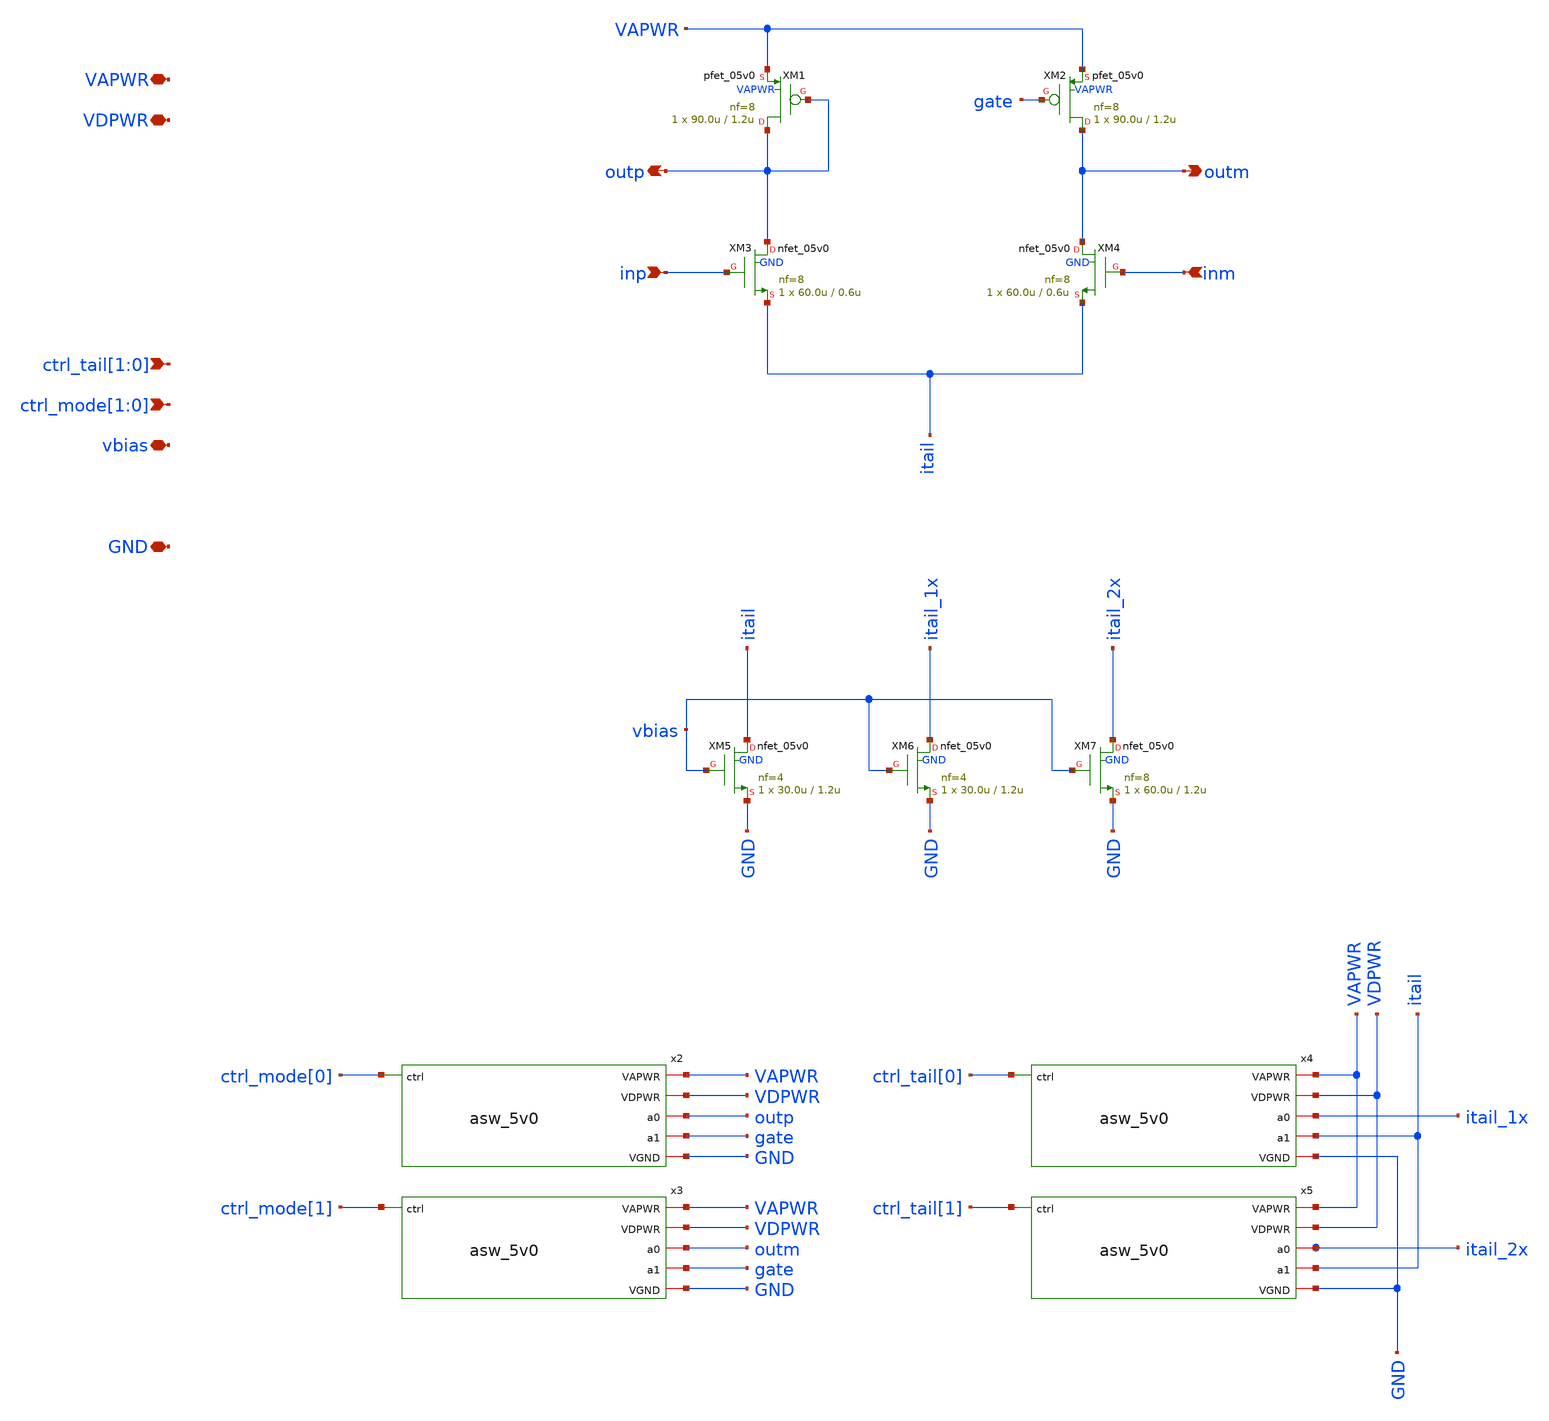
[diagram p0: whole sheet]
** sch_path: xschem/ota_n.sch
**.subckt ota_n vbias ctrl_tail[1],ctrl_tail[0] VAPWR VDPWR GND ctrl_mode[1],ctrl_mode[0] inp inm
*+ outp outm
*.iopin vbias
*.ipin ctrl_tail[1],ctrl_tail[0]
*.iopin VAPWR
*.iopin VDPWR
*.iopin GND
*.ipin ctrl_mode[1],ctrl_mode[0]
*.ipin inp
*.ipin inm
*.opin outp
*.opin outm
x2 GND VDPWR VAPWR ctrl_mode[0] outp gate asw_5v0
x3 GND VDPWR VAPWR ctrl_mode[1] outm gate asw_5v0
x4 GND VDPWR VAPWR ctrl_tail[0] itail_1x itail asw_5v0
x5 GND VDPWR VAPWR ctrl_tail[1] itail_2x itail asw_5v0
XM5 itail vbias GND GND nfet_05v0 L=1.2u W=30.0u nf=4 ad='int((nf+1)/2) * W/nf * 0.18u' as='int((nf+2)/2) * W/nf * 0.18u'
+ pd='2*int((nf+1)/2) * (W/nf + 0.18u)' ps='2*int((nf+2)/2) * (W/nf + 0.18u)' nrd='0.18u / W' nrs='0.18u / W'
+ sa=0 sb=0 sd=0 m=1 par=1
XM6 itail_1x vbias GND GND nfet_05v0 L=1.2u W=30.0u nf=4 ad='int((nf+1)/2) * W/nf * 0.18u' as='int((nf+2)/2) * W/nf * 0.18u'
+ pd='2*int((nf+1)/2) * (W/nf + 0.18u)' ps='2*int((nf+2)/2) * (W/nf + 0.18u)' nrd='0.18u / W' nrs='0.18u / W'
+ sa=0 sb=0 sd=0 m=1 par=1
XM7 itail_2x vbias GND GND nfet_05v0 L=1.2u W=60.0u nf=8 ad='int((nf+1)/2) * W/nf * 0.18u' as='int((nf+2)/2) * W/nf * 0.18u'
+ pd='2*int((nf+1)/2) * (W/nf + 0.18u)' ps='2*int((nf+2)/2) * (W/nf + 0.18u)' nrd='0.18u / W' nrs='0.18u / W'
+ sa=0 sb=0 sd=0 m=1 par=1
XM1 outp outp VAPWR VAPWR pfet_05v0 L=1.2u W=90.0u nf=8 ad='int((nf+1)/2) * W/nf * 0.18u' as='int((nf+2)/2) * W/nf * 0.18u'
+ pd='2*int((nf+1)/2) * (W/nf + 0.18u)' ps='2*int((nf+2)/2) * (W/nf + 0.18u)' nrd='0.18u / W' nrs='0.18u / W'
+ sa=0 sb=0 sd=0 m=1 par=1
XM2 outm gate VAPWR VAPWR pfet_05v0 L=1.2u W=90.0u nf=8 ad='int((nf+1)/2) * W/nf * 0.18u' as='int((nf+2)/2) * W/nf * 0.18u'
+ pd='2*int((nf+1)/2) * (W/nf + 0.18u)' ps='2*int((nf+2)/2) * (W/nf + 0.18u)' nrd='0.18u / W' nrs='0.18u / W'
+ sa=0 sb=0 sd=0 m=1 par=1
XM3 outp inp itail GND nfet_05v0 L=0.6u W=60.0u nf=8 ad='int((nf+1)/2) * W/nf * 0.18u' as='int((nf+2)/2) * W/nf * 0.18u'
+ pd='2*int((nf+1)/2) * (W/nf + 0.18u)' ps='2*int((nf+2)/2) * (W/nf + 0.18u)' nrd='0.18u / W' nrs='0.18u / W'
+ sa=0 sb=0 sd=0 m=1 par=1
XM4 outm inm itail GND nfet_05v0 L=0.6u W=60.0u nf=8 ad='int((nf+1)/2) * W/nf * 0.18u' as='int((nf+2)/2) * W/nf * 0.18u'
+ pd='2*int((nf+1)/2) * (W/nf + 0.18u)' ps='2*int((nf+2)/2) * (W/nf + 0.18u)' nrd='0.18u / W' nrs='0.18u / W'
+ sa=0 sb=0 sd=0 m=1 par=1
**.ends

* expanding   symbol:  asw_5v0.sym # of pins=6
** sym_path: xschem/asw_5v0.sym
** sch_path: xschem/asw_5v0.sch
.subckt asw_5v0 VGND VDPWR VAPWR ctrl a0 a1
*.ipin ctrl
*.iopin VDPWR
*.iopin VGND
*.iopin a0
*.iopin VAPWR
*.iopin a1
x1 VGND VDPWR VAPWR ctrl tgon_p tgon_n lv2hv
XM1 a0 tgon_n a1 VAPWR pfet_05v0 L=0.50u W=592u nf=16 ad='int((nf+1)/2) * W/nf * 0.18u' as='int((nf+2)/2) * W/nf * 0.18u'
+ pd='2*int((nf+1)/2) * (W/nf + 0.18u)' ps='2*int((nf+2)/2) * (W/nf + 0.18u)' nrd='0.18u / W' nrs='0.18u / W'
+ sa=0 sb=0 sd=0 m=1 par=1
XM2 a1 tgon_p a0 VGND nfet_05v0 L=0.60u W=248u nf=8 ad='int((nf+1)/2) * W/nf * 0.18u' as='int((nf+2)/2) * W/nf * 0.18u'
+ pd='2*int((nf+1)/2) * (W/nf + 0.18u)' ps='2*int((nf+2)/2) * (W/nf + 0.18u)' nrd='0.18u / W' nrs='0.18u / W'
+ sa=0 sb=0 sd=0 m=1 par=1
.ends


* expanding   symbol:  lv2hv.sym # of pins=6
** sym_path: lv2hv.sym
** sch_path: lv2hv.sch
.subckt lv2hv VGND VDPWR VAPWR in out_p out_n
*.iopin VAPWR
*.iopin VGND
*.ipin in
*.iopin VDPWR
*.opin out_p
*.opin out_n
XM1 in_n in VGND VGND nfet_03v3 L=0.28u W=0.89u nf=1 ad='int((nf+1)/2) * W/nf * 0.18u' as='int((nf+2)/2) * W/nf * 0.18u'
+ pd='2*int((nf+1)/2) * (W/nf + 0.18u)' ps='2*int((nf+2)/2) * (W/nf + 0.18u)' nrd='0.18u / W' nrs='0.18u / W'
+ sa=0 sb=0 sd=0 m=1 par=1
XM2 in_n in VDPWR VDPWR pfet_03v3 L=0.28u W=2.0u nf=1 ad='int((nf+1)/2) * W/nf * 0.18u' as='int((nf+2)/2) * W/nf * 0.18u'
+ pd='2*int((nf+1)/2) * (W/nf + 0.18u)' ps='2*int((nf+2)/2) * (W/nf + 0.18u)' nrd='0.18u / W' nrs='0.18u / W'
+ sa=0 sb=0 sd=0 m=1 par=1
XM3 VGND in_p net1 VGND nfet_05v0 L=0.6u W=0.5u nf=1 ad='int((nf+1)/2) * W/nf * 0.18u' as='int((nf+2)/2) * W/nf * 0.18u'
+ pd='2*int((nf+1)/2) * (W/nf + 0.18u)' ps='2*int((nf+2)/2) * (W/nf + 0.18u)' nrd='0.18u / W' nrs='0.18u / W'
+ sa=0 sb=0 sd=0 m=1 par=1
XM4 net1 net2 VAPWR VAPWR pfet_05v0 L=0.5u W=0.5u nf=1 ad='int((nf+1)/2) * W/nf * 0.18u' as='int((nf+2)/2) * W/nf * 0.18u'
+ pd='2*int((nf+1)/2) * (W/nf + 0.18u)' ps='2*int((nf+2)/2) * (W/nf + 0.18u)' nrd='0.18u / W' nrs='0.18u / W'
+ sa=0 sb=0 sd=0 m=1 par=1
XM5 net2 in_n VGND VGND nfet_05v0 L=0.6u W=0.5u nf=1 ad='int((nf+1)/2) * W/nf * 0.18u' as='int((nf+2)/2) * W/nf * 0.18u'
+ pd='2*int((nf+1)/2) * (W/nf + 0.18u)' ps='2*int((nf+2)/2) * (W/nf + 0.18u)' nrd='0.18u / W' nrs='0.18u / W'
+ sa=0 sb=0 sd=0 m=1 par=1
XM6 net2 net1 VAPWR VAPWR pfet_05v0 L=0.5u W=0.5u nf=1 ad='int((nf+1)/2) * W/nf * 0.18u' as='int((nf+2)/2) * W/nf * 0.18u'
+ pd='2*int((nf+1)/2) * (W/nf + 0.18u)' ps='2*int((nf+2)/2) * (W/nf + 0.18u)' nrd='0.18u / W' nrs='0.18u / W'
+ sa=0 sb=0 sd=0 m=1 par=1
XM7 VGND net2 out_n VGND nfet_05v0 L=0.60u W=0.5u nf=1 ad='int((nf+1)/2) * W/nf * 0.18u' as='int((nf+2)/2) * W/nf * 0.18u'
+ pd='2*int((nf+1)/2) * (W/nf + 0.18u)' ps='2*int((nf+2)/2) * (W/nf + 0.18u)' nrd='0.18u / W' nrs='0.18u / W'
+ sa=0 sb=0 sd=0 m=1 par=1
XM8 out_n net2 VAPWR VAPWR pfet_05v0 L=0.5u W=1.0u nf=2 ad='int((nf+1)/2) * W/nf * 0.18u' as='int((nf+2)/2) * W/nf * 0.18u'
+ pd='2*int((nf+1)/2) * (W/nf + 0.18u)' ps='2*int((nf+2)/2) * (W/nf + 0.18u)' nrd='0.18u / W' nrs='0.18u / W'
+ sa=0 sb=0 sd=0 m=1 par=1
XM9 VGND net1 out_p VGND nfet_05v0 L=0.60u W=0.5u nf=1 ad='int((nf+1)/2) * W/nf * 0.18u' as='int((nf+2)/2) * W/nf * 0.18u'
+ pd='2*int((nf+1)/2) * (W/nf + 0.18u)' ps='2*int((nf+2)/2) * (W/nf + 0.18u)' nrd='0.18u / W' nrs='0.18u / W'
+ sa=0 sb=0 sd=0 m=1 par=1
XM10 out_p net1 VAPWR VAPWR pfet_05v0 L=0.5u W=1.0u nf=2 ad='int((nf+1)/2) * W/nf * 0.18u' as='int((nf+2)/2) * W/nf * 0.18u'
+ pd='2*int((nf+1)/2) * (W/nf + 0.18u)' ps='2*int((nf+2)/2) * (W/nf + 0.18u)' nrd='0.18u / W' nrs='0.18u / W'
+ sa=0 sb=0 sd=0 m=1 par=1
XM11 in_p in_n VGND VGND nfet_03v3 L=0.28u W=0.89u nf=1 ad='int((nf+1)/2) * W/nf * 0.18u' as='int((nf+2)/2) * W/nf * 0.18u'
+ pd='2*int((nf+1)/2) * (W/nf + 0.18u)' ps='2*int((nf+2)/2) * (W/nf + 0.18u)' nrd='0.18u / W' nrs='0.18u / W'
+ sa=0 sb=0 sd=0 m=1 par=1
XM12 in_p in_n VDPWR VDPWR pfet_03v3 L=0.28u W=2.0u nf=1 ad='int((nf+1)/2) * W/nf * 0.18u' as='int((nf+2)/2) * W/nf * 0.18u'
+ pd='2*int((nf+1)/2) * (W/nf + 0.18u)' ps='2*int((nf+2)/2) * (W/nf + 0.18u)' nrd='0.18u / W' nrs='0.18u / W'
+ sa=0 sb=0 sd=0 m=1 par=1
.ends

.end
